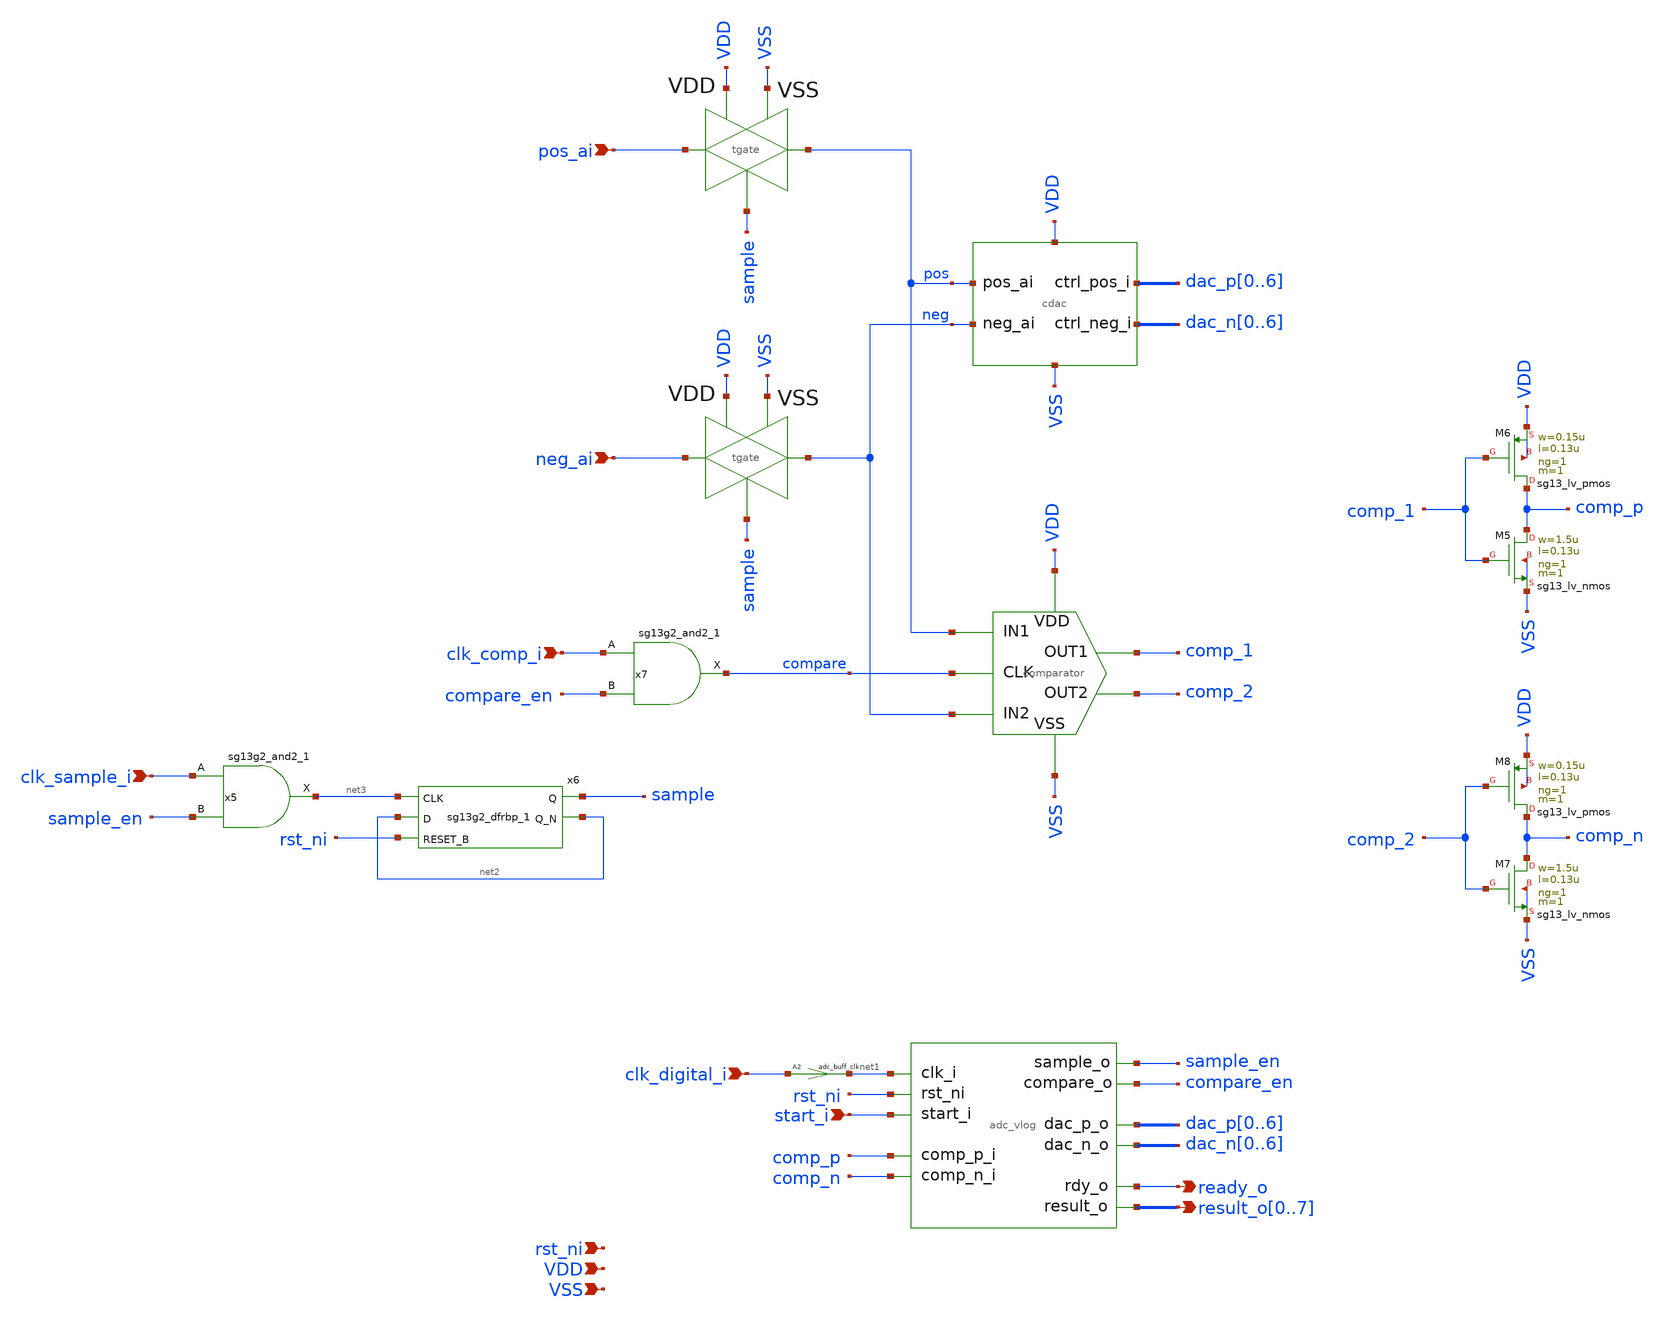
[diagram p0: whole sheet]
** sch_path: xschem/adc.sch
* IHP-GmbH/IHP-Open-PDK/ihp-sg13g2/libs.tech/xschem/sg13g2_stdcells/sg13g2_buf_1.sch:
* Copyright 2023 IHP PDK Authors
* Licensed under the Apache License, Version 2.0 (the "License");
**.subckt adc pos_ai clk_digital_i VSS VDD start_i ready_o
*+ result_o0,result_o1,result_o2,result_o3,result_o4,result_o5,result_o6,result_o7 clk_comp_i neg_ai clk_sample_i rst_ni
*.ipin pos_ai
*.ipin clk_digital_i
*.ipin VSS
*.ipin VDD
*.ipin start_i
*.opin ready_o
*.opin result_o0,result_o1,result_o2,result_o3,result_o4,result_o5,result_o6,result_o7
*.ipin clk_comp_i
*.ipin neg_ai
*.ipin clk_sample_i
*.ipin rst_ni
x1 sample pos_ai pos VDD VSS tgate
a1 [ net1 start_i rst_ni comp_p comp_n ] [ compare_en sample_en dac_p0 dac_p1 dac_p2 dac_p3 dac_p4
+ dac_p5 dac_p6 dac_n0 dac_n1 dac_n2 dac_n3 dac_n4 dac_n5 dac_n6 ready_o result_o0 result_o1 result_o2
+ result_o3 result_o4 result_o5 result_o6 result_o7 ] adc
x2 compare pos neg comp_2 comp_1 VSS VDD comparator
x3 sample neg_ai neg VDD VSS tgate
x4 pos neg VSS VDD dac_p0 dac_p1 dac_p2 dac_p3 dac_p4 dac_p5 dac_p6 dac_n0 dac_n1 dac_n2 dac_n3
+ dac_n4 dac_n5 dac_n6 cdac
XM5 comp_p comp_1 VSS VSS sg13_lv_nmos w=1.5u l=0.13u ng=1 m=1 mm_ok=1
XM6 comp_p comp_1 VDD VDD sg13_lv_pmos w=0.15u l=0.13u ng=1 m=1 mm_ok=1
XM7 comp_n comp_2 VSS VSS sg13_lv_nmos w=1.5u l=0.13u ng=1 m=1 mm_ok=1
XM8 comp_n comp_2 VDD VDD sg13_lv_pmos w=0.15u l=0.13u ng=1 m=1 mm_ok=1
x6 sample net2 net3 net2 rst_ni VDD VSS sg13g2_dfrbp_1
x5 net3 clk_sample_i sample_en VDD VSS sg13g2_and2_1
A2 [ clk_digital_i ] [ net1 ] adc_buff_clk
x7 compare clk_comp_i compare_en VDD VSS sg13g2_and2_1
**.ends

* expanding   symbol:  ./tgate.sym # of pins=5
** sym_path: xschem/tgate.sym
** sch_path: xschem/tgate.sch
.subckt tgate CTRL A B VDD VSS
*.ipin CTRL
*.ipin VDD
*.ipin VSS
*.iopin B
*.iopin A
x1 ctrl_ni CTRL VDD VSS sg13g2_inv_1
x2 ctrl_i CTRL VDD VSS sg13g2_buf_1
XM3 B ctrl_i A VSS sg13_lv_nmos w=3.41u l=0.13u ng=1 m=1 mm_ok=1
XM1 A ctrl_ni B VDD sg13_lv_pmos w=8.82u l=0.13u ng=1 m=1 mm_ok=1
.ends


* expanding   symbol:  ./comparator.sym # of pins=7
** sym_path: xschem/comparator.sym
** sch_path: xschem/comparator.sch
.subckt comparator CLK IN1 IN2 OUT2 OUT1 VSS VDD
*.ipin CLK
*.ipin IN1
*.ipin IN2
*.opin OUT2
*.opin OUT1
*.ipin VSS
*.ipin VDD
XM1 P CLK VDD VDD sg13_lv_pmos w=2u l=0.13u ng=1 m=1 mm_ok=1
XM3 OUT1 OUT2 VDD VDD sg13_lv_pmos w=1u l=0.13u ng=1 m=1 mm_ok=1
XM4 OUT2 OUT1 VDD VDD sg13_lv_pmos w=1u l=0.13u ng=1 m=1 mm_ok=1
XM8 OUT1 OUT2 P VSS sg13_lv_nmos w=1u l=0.13u ng=1 m=1 mm_ok=1
XM9 P IN1 S VSS sg13_lv_nmos w=12u l=0.13u ng=6 m=1 mm_ok=1
XM11 S CLK VSS VSS sg13_lv_nmos w=4u l=2u ng=2 m=1 mm_ok=1
XM10 N IN2 S VSS sg13_lv_nmos w=12u l=0.13u ng=6 m=1 mm_ok=1
XM2 OUT1 CLK VDD VDD sg13_lv_pmos w=2u l=0.13u ng=1 m=1 mm_ok=1
XM5 N CLK VDD VDD sg13_lv_pmos w=2u l=0.13u ng=1 m=1 mm_ok=1
XM6 OUT2 CLK VDD VDD sg13_lv_pmos w=2u l=0.13u ng=1 m=1 mm_ok=1
XM7 OUT2 OUT1 N VSS sg13_lv_nmos w=1u l=0.13u ng=1 m=1 mm_ok=1
XC2 OUT1 VSS cap_cmim w=1.8e-6 l=1.8e-6 m=1 mm_ok=1
XC4 OUT2 VSS cap_cmim w=1.8e-6 l=1.8e-6 m=1 mm_ok=1
XC1 P VSS cap_cmim w=3e-6 l=3e-6 m=1 mm_ok=1
XC3 N VSS cap_cmim w=3e-6 l=3e-6 m=1 mm_ok=1
C5 S VSS 25f m=1
.ends


* expanding   symbol:  ./cdac.sym # of pins=6
** sym_path: xschem/cdac.sym
** sch_path: xschem/cdac.sch
.subckt cdac pos_ai neg_ai VSS VDD pos_ctrl_i0 pos_ctrl_i1 pos_ctrl_i2 pos_ctrl_i3 pos_ctrl_i4
+ pos_ctrl_i5 pos_ctrl_i6 neg_ctrl_i0 neg_ctrl_i1 neg_ctrl_i2 neg_ctrl_i3 neg_ctrl_i4 neg_ctrl_i5 neg_ctrl_i6
*.ipin pos_ai
*.ipin VSS
*.ipin VDD
*.ipin neg_ai
*.ipin pos_ctrl_i0,pos_ctrl_i1,pos_ctrl_i2,pos_ctrl_i3,pos_ctrl_i4,pos_ctrl_i5,pos_ctrl_i6
*.ipin neg_ctrl_i0,neg_ctrl_i1,neg_ctrl_i2,neg_ctrl_i3,neg_ctrl_i4,neg_ctrl_i5,neg_ctrl_i6
x2 net1 pos_ctrl_i0 VDD VSS sg13g2_inv_2
x3 net2 pos_ctrl_i1 VDD VSS sg13g2_inv_2
x4 net3 pos_ctrl_i2 VDD VSS sg13g2_inv_2
x5 net4 pos_ctrl_i3 VDD VSS sg13g2_inv_2
x6 net5 pos_ctrl_i4 VDD VSS sg13g2_inv_2
x7 net6 pos_ctrl_i5 VDD VSS sg13g2_inv_2
x8 net7 pos_ctrl_i6 VDD VSS sg13g2_inv_2
XC1 pos_ai net7 cap_cmim w={s} l={s} m=1 mm_ok=1
XC2 pos_ai net6 cap_cmim w={s} l={s} m=2 mm_ok=1
XC3 pos_ai net5 cap_cmim w={s} l={s} m=4 mm_ok=1
x10 net8 neg_ctrl_i0 VDD VSS sg13g2_inv_2
x11 net9 neg_ctrl_i1 VDD VSS sg13g2_inv_2
x12 net10 neg_ctrl_i2 VDD VSS sg13g2_inv_2
x13 net11 neg_ctrl_i3 VDD VSS sg13g2_inv_2
x14 net12 neg_ctrl_i4 VDD VSS sg13g2_inv_2
x15 net13 neg_ctrl_i5 VDD VSS sg13g2_inv_2
x16 net14 neg_ctrl_i6 VDD VSS sg13g2_inv_2
XC10 neg_ai net14 cap_cmim w={s} l={s} m=1 mm_ok=1
XC11 neg_ai net13 cap_cmim w={s} l={s} m=2 mm_ok=1
XC12 neg_ai net12 cap_cmim w={s} l={s} m=4 mm_ok=1
* noconn VDD
.param s=2.5292e-6
x1 net15 neg_ctrl_i0 VDD VSS sg13g2_buf_2
x9 net16 pos_ctrl_i0 VDD VSS sg13g2_buf_2
XC7 pos_ai net1 cap_cmim w={s} l={s} m=32 mm_ok=1
XC9 neg_ai net16 cap_cmim w={s} l={s} m=32 mm_ok=1
XC13 neg_ai net8 cap_cmim w={s} l={s} m=32 mm_ok=1
XC16 pos_ai net15 cap_cmim w={s} l={s} m=32 mm_ok=1
x17 net17 neg_ctrl_i1 VDD VSS sg13g2_buf_2
x18 net18 pos_ctrl_i1 VDD VSS sg13g2_buf_2
XC17 neg_ai net18 cap_cmim w={s} l={s} m=16 mm_ok=1
XC18 pos_ai net17 cap_cmim w={s} l={s} m=16 mm_ok=1
XC4 neg_ai net9 cap_cmim w={s} l={s} m=16 mm_ok=1
XC8 pos_ai net2 cap_cmim w={s} l={s} m=16 mm_ok=1
x19 net19 neg_ctrl_i2 VDD VSS sg13g2_buf_2
x20 net20 pos_ctrl_i2 VDD VSS sg13g2_buf_2
XC19 pos_ai net19 cap_cmim w={s} l={s} m=8 mm_ok=1
XC6 neg_ai net10 cap_cmim w={s} l={s} m=8 mm_ok=1
XC15 pos_ai net3 cap_cmim w={s} l={s} m=8 mm_ok=1
XC20 neg_ai net20 cap_cmim w={s} l={s} m=8 mm_ok=1
x21 net21 neg_ctrl_i3 VDD VSS sg13g2_buf_2
x22 net22 pos_ctrl_i3 VDD VSS sg13g2_buf_2
XC5 pos_ai net4 cap_cmim w={s} l={s} m=4 mm_ok=1
XC14 neg_ai net22 cap_cmim w={s} l={s} m=4 mm_ok=1
XC21 neg_ai net11 cap_cmim w={s} l={s} m=4 mm_ok=1
XC22 pos_ai net21 cap_cmim w={s} l={s} m=4 mm_ok=1
XC23 neg_ai VSS cap_cmim w={s} l={s} m=47.54545455 mm_ok=1
XC24 pos_ai VSS cap_cmim w={s} l={s} m=47.54545455 mm_ok=1
.ends


* expanding   symbol:  sg13g2_stdcells/sg13g2_dfrbp_1.sym # of pins=5
** sym_path: sg13g2_stdcells/sg13g2_dfrbp_1.sym
** sch_path: sg13g2_stdcells/sg13g2_dfrbp_1.sch
.subckt sg13g2_dfrbp_1 Q Q_N CLK D RESET_B VDD VSS
*.ipin D
*.ipin RESET_B
*.ipin CLK
*.opin Q
*.opin Q_N
*.iopin VDD
*.iopin VSS
XM1 Db D net10 VSS sg13_lv_nmos w=420.00n l=130.00n ng=1 m=1 mm_ok=1
XM2 net10 RESET_B VSS VSS sg13_lv_nmos w=420.00n l=130.00n ng=1 m=1 mm_ok=1
XM3 net1 clkneg net9 VSS sg13_lv_nmos w=420.00n l=130.00n ng=1 m=1 mm_ok=1
XM4 net9 net1 VSS VSS sg13_lv_nmos w=420.00n l=130.00n ng=1 m=1 mm_ok=1
XM5 net1 net1 net5 VSS sg13_lv_nmos w=420.00n l=130.00n ng=1 m=1 mm_ok=1
XM6 net5 RESET_B VSS VSS sg13_lv_nmos w=420.00n l=130.00n ng=1 m=1 mm_ok=1
XM7 Q_N net1 VSS VSS sg13_lv_nmos w=740.00n l=130.00n ng=1 m=1 mm_ok=1
XM8 net2 net1 VSS VSS sg13_lv_nmos w=740.00n l=130.00n ng=1 m=1 mm_ok=1
XM9 Q net2 VSS VSS sg13_lv_nmos w=740.00n l=130.00n ng=1 m=1 mm_ok=1
XM10 clkneg CLK VSS VSS sg13_lv_nmos w=740.00n l=130.00n ng=1 m=1 mm_ok=1
XM11 clkpos clkneg VSS VSS sg13_lv_nmos w=740.00n l=130.00n ng=1 m=1 mm_ok=1
XM12 Db clkneg net3 VSS sg13_lv_nmos w=420.00n l=130.00n ng=1 m=1 mm_ok=1
XM13 net3 clkpos net8 VSS sg13_lv_nmos w=420.00n l=130.00n ng=1 m=1 mm_ok=1
XM14 net8 net3 net4 VSS sg13_lv_nmos w=420.00n l=130.00n ng=1 m=1 mm_ok=1
XM15 net4 RESET_B VSS VSS sg13_lv_nmos w=420.00n l=130.00n ng=1 m=1 mm_ok=1
XM16 net3 net3 VSS VSS sg13_lv_nmos w=740.00n l=130.00n ng=1 m=1 mm_ok=1
XM17 net3 clkpos net1 VSS sg13_lv_nmos w=740.00n l=130.00n ng=1 m=1 mm_ok=1
XM18 Db RESET_B VDD VDD sg13_lv_pmos w=420.00n l=130.00n ng=1 m=1 mm_ok=1
XM19 Db D VDD VDD sg13_lv_pmos w=420.00n l=130.00n ng=1 m=1 mm_ok=1
XM20 net7 net1 VDD VDD sg13_lv_pmos w=420.00n l=130.00n ng=1 m=1 mm_ok=1
XM21 net1 clkpos net7 VDD sg13_lv_pmos w=420.00n l=130.00n ng=1 m=1 mm_ok=1
XM22 net1 net1 VDD VDD sg13_lv_pmos w=420.00n l=130.00n ng=1 m=1 mm_ok=1
XM23 net1 RESET_B VDD VDD sg13_lv_pmos w=420.00n l=130.00n ng=1 m=1 mm_ok=1
XM24 Q_N net1 VDD VDD sg13_lv_pmos w=1.12u l=130.00n ng=1 m=1 mm_ok=1
XM25 net2 net1 VDD VDD sg13_lv_pmos w=1.12u l=130.00n ng=1 m=1 mm_ok=1
XM26 Q net2 VDD VDD sg13_lv_pmos w=1.12u l=130.00n ng=1 m=1 mm_ok=1
XM27 clkneg CLK VDD VDD sg13_lv_pmos w=1.12u l=130.00n ng=1 m=1 mm_ok=1
XM28 clkpos clkneg VDD VDD sg13_lv_pmos w=1.12u l=130.00n ng=1 m=1 mm_ok=1
XM29 Db clkpos net3 VDD sg13_lv_pmos w=420.00n l=130.00n ng=1 m=1 mm_ok=1
XM30 net6 net3 VDD VDD sg13_lv_pmos w=420.00n l=130.00n ng=1 m=1 mm_ok=1
XM31 net3 clkneg net6 VDD sg13_lv_pmos w=420.00n l=130.00n ng=1 m=1 mm_ok=1
XM32 net3 RESET_B VDD VDD sg13_lv_pmos w=420.00n l=130.00n ng=1 m=1 mm_ok=1
XM33 net3 net3 VDD VDD sg13_lv_pmos w=1.000u l=130.00n ng=1 m=1 mm_ok=1
XM34 net3 clkneg net1 VDD sg13_lv_pmos w=1.000u l=130.00n ng=1 m=1 mm_ok=1
.ends


* expanding   symbol:  sg13g2_stdcells/sg13g2_and2_1.sym # of pins=3
** sym_path: sg13g2_stdcells/sg13g2_and2_1.sym
** sch_path: sg13g2_stdcells/sg13g2_and2_1.sch
.subckt sg13g2_and2_1 X A B VDD VSS
*.ipin A
*.ipin B
*.opin X
*.iopin VDD
*.iopin VSS
XM1 net1 A net2 VSS sg13_lv_nmos w=640.00n l=130.00n ng=1 m=1 mm_ok=1
XM2 net2 B VSS VSS sg13_lv_nmos w=640.00n l=130.00n ng=1 m=1 mm_ok=1
XM3 X net1 VSS VSS sg13_lv_nmos w=740.00n l=130.00n ng=1 m=1 mm_ok=1
XM4 net1 B VDD VDD sg13_lv_pmos w=840.00n l=130.00n ng=1 m=1 mm_ok=1
XM5 net1 A VDD VDD sg13_lv_pmos w=840.00n l=130.00n ng=1 m=1 mm_ok=1
XM6 X net1 VDD VDD sg13_lv_pmos w=1.12u l=130.00n ng=1 m=1 mm_ok=1
.ends


* expanding   symbol:  sg13g2_stdcells/sg13g2_inv_1.sym # of pins=2
** sym_path: sg13g2_stdcells/sg13g2_inv_1.sym
** sch_path: sg13g2_stdcells/sg13g2_inv_1.sch
.subckt sg13g2_inv_1 Y A VDD VSS
*.opin Y
*.ipin A
*.iopin VDD
*.iopin VSS
XM1 Y A VSS VSS sg13_lv_nmos w=740.00n l=130.00n ng=1 m=1 mm_ok=1
XM2 Y A VDD VDD sg13_lv_pmos w=1.12u l=130.00n ng=1 m=1 mm_ok=1
.ends


* expanding   symbol:  sg13g2_stdcells/sg13g2_buf_1.sym # of pins=2
** sym_path: sg13g2_stdcells/sg13g2_buf_1.sym
** sch_path: sg13g2_stdcells/sg13g2_buf_1.sch
.subckt sg13g2_buf_1 X A VDD VSS
*.ipin A
*.opin X
*.iopin VDD
*.iopin VSS
XM1 net1 A VSS VSS sg13_lv_nmos w=550.00n l=130.00n ng=1 m=1 mm_ok=1
XM2 X net1 VSS VSS sg13_lv_nmos w=740.00n l=130.00n ng=1 m=1 mm_ok=1
XM3 net1 A VDD VDD sg13_lv_pmos w=840.00n l=130.00n ng=1 m=1 mm_ok=1
XM4 X net1 VDD VDD sg13_lv_pmos w=1.12u l=130.00n ng=1 m=1 mm_ok=1
.ends


* expanding   symbol:  sg13g2_stdcells/sg13g2_inv_2.sym # of pins=2
** sym_path: sg13g2_stdcells/sg13g2_inv_2.sym
** sch_path: sg13g2_stdcells/sg13g2_inv_2.sch
.subckt sg13g2_inv_2 Y A VDD VSS
*.opin Y
*.ipin A
*.iopin VDD
*.iopin VSS
XM1 Y A VSS VSS sg13_lv_nmos w=1.48u l=130.00n ng=2 m=1 mm_ok=1
XM2 Y A VDD VDD sg13_lv_pmos w=2.24u l=130.00n ng=2 m=1 mm_ok=1
.ends


* expanding   symbol:  sg13g2_stdcells/sg13g2_buf_2.sym # of pins=2
** sym_path: sg13g2_stdcells/sg13g2_buf_2.sym
** sch_path: sg13g2_stdcells/sg13g2_buf_2.sch
.subckt sg13g2_buf_2 X A VDD VSS
*.ipin A
*.opin X
*.iopin VDD
*.iopin VSS
XM1 net1 A VSS VSS sg13_lv_nmos w=640.00n l=130.00n ng=1 m=1 mm_ok=1
XM2 X net1 VSS VSS sg13_lv_nmos w=1.48u l=130.00n ng=2 m=1 mm_ok=1
XM3 net1 A VDD VDD sg13_lv_pmos w=1.000u l=130.00n ng=1 m=1 mm_ok=1
XM4 X net1 VDD VDD sg13_lv_pmos w=2.24u l=130.00n ng=2 m=1 mm_ok=1
.ends

**** begin user architecture code
.model adc d_cosim simulation="ivlng" sim_args=["adc"]
**** end user architecture code
.end
